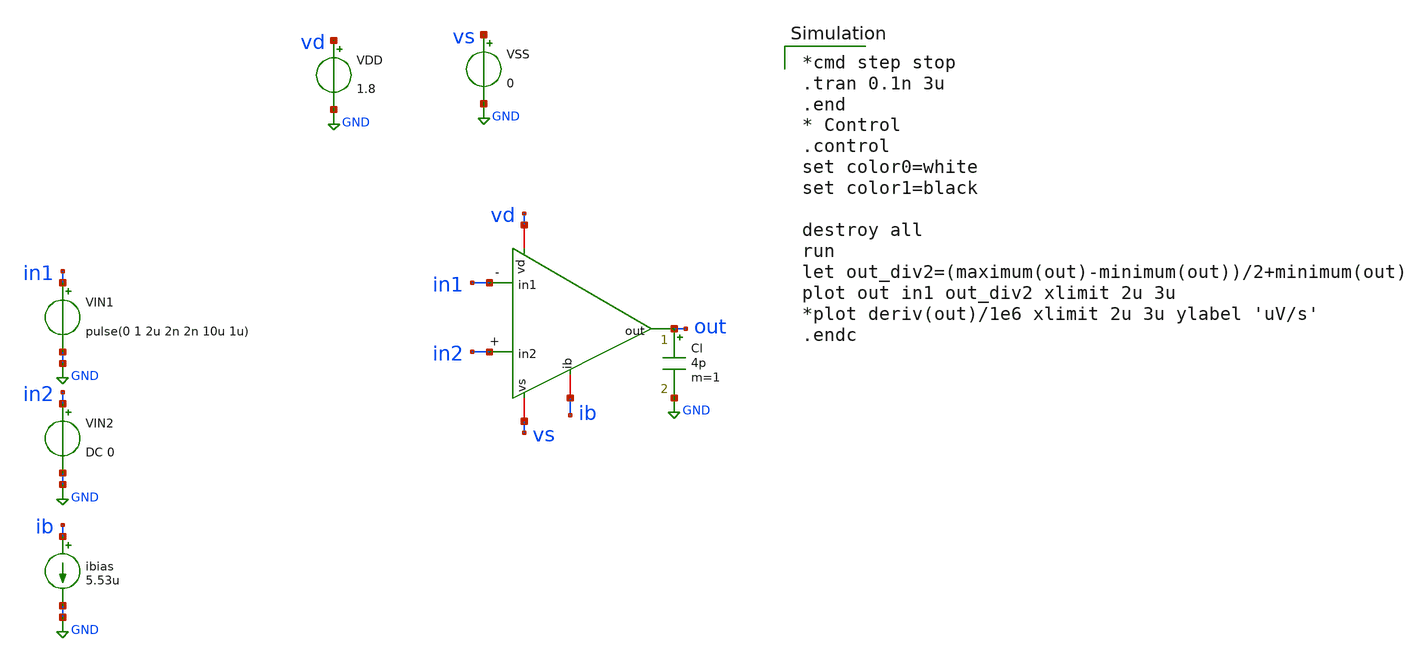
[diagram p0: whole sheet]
** sch_path: amp-op/xschem/ampop_tb-largesignal.sch
* Copyright 2020 Stefan Frederik Schippers
* Licensed under the Apache License, Version 2.0 (the "License");
* you may not use this file except in compliance with the License.
* You may obtain a copy of the License at
* https://www.apache.org/licenses/LICENSE-2.0
* Unless required by applicable law or agreed to in writing, software
* distributed under the License is distributed on an "AS IS" BASIS,
* WITHOUT WARRANTIES OR CONDITIONS OF ANY KIND, either express or implied.
* See the License for the specific language governing permissions and
* limitations under the License.
**.subckt ampop_tb-largesignal
VIN2 in2 GND DC 0
VIN1 in1 GND pulse(0 1 2u 2n 2n 10u 1u)
ibias ib GND 5.53u
VDD vd GND 1.8
VSS vs GND 0
Cl out GND 4p m=1
x1 vd in1 in2 out ib vs ampop
**** begin user architecture code

*cmd step stop
.tran 0.1n 3u
.end
* Control
.control
set color0=white
set color1=black

destroy all
run
let out_div2=(maximum(out)-minimum(out))/2+minimum(out)
plot out in1 out_div2 xlimit 2u 3u
*plot deriv(out)/1e6 xlimit 2u 3u ylabel 'uV/s'
.endc

 .lib $::SKYWATER_MODELS/sky130.lib.spice tt
.include $::SKYWATER_STDCELLS/sky130_fd_sc_hd.spice

**** end user architecture code
**.ends
.GLOBAL GND
.end
